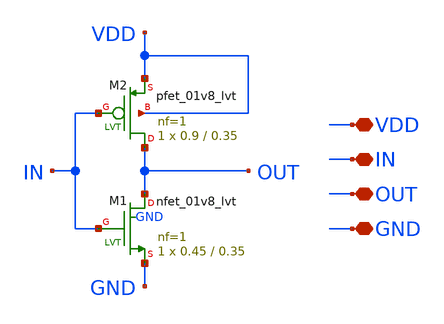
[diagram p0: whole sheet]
** sch_path: LVT/inv_LVT/inv_LVT.sch
**.subckt inv_LVT VDD IN OUT GND
*.iopin VDD
*.iopin IN
*.iopin OUT
*.iopin GND
XM1 OUT IN GND GND sky130_fd_pr__nfet_01v8_lvt L=0.35 W=0.45 nf=1 ad='int((nf+1)/2) * W/nf * 0.29' as='int((nf+2)/2) * W/nf * 0.29'
+ pd='2*int((nf+1)/2) * (W/nf + 0.29)' ps='2*int((nf+2)/2) * (W/nf + 0.29)' nrd='0.29 / W' nrs='0.29 / W'
+ sa=0 sb=0 sd=0 mult=1 m=1
XM2 OUT IN VDD VDD sky130_fd_pr__pfet_01v8_lvt L=0.35 W=0.9 nf=1 ad='int((nf+1)/2) * W/nf * 0.29' as='int((nf+2)/2) * W/nf * 0.29'
+ pd='2*int((nf+1)/2) * (W/nf + 0.29)' ps='2*int((nf+2)/2) * (W/nf + 0.29)' nrd='0.29 / W' nrs='0.29 / W'
+ sa=0 sb=0 sd=0 mult=1 m=1
**.ends
.end
